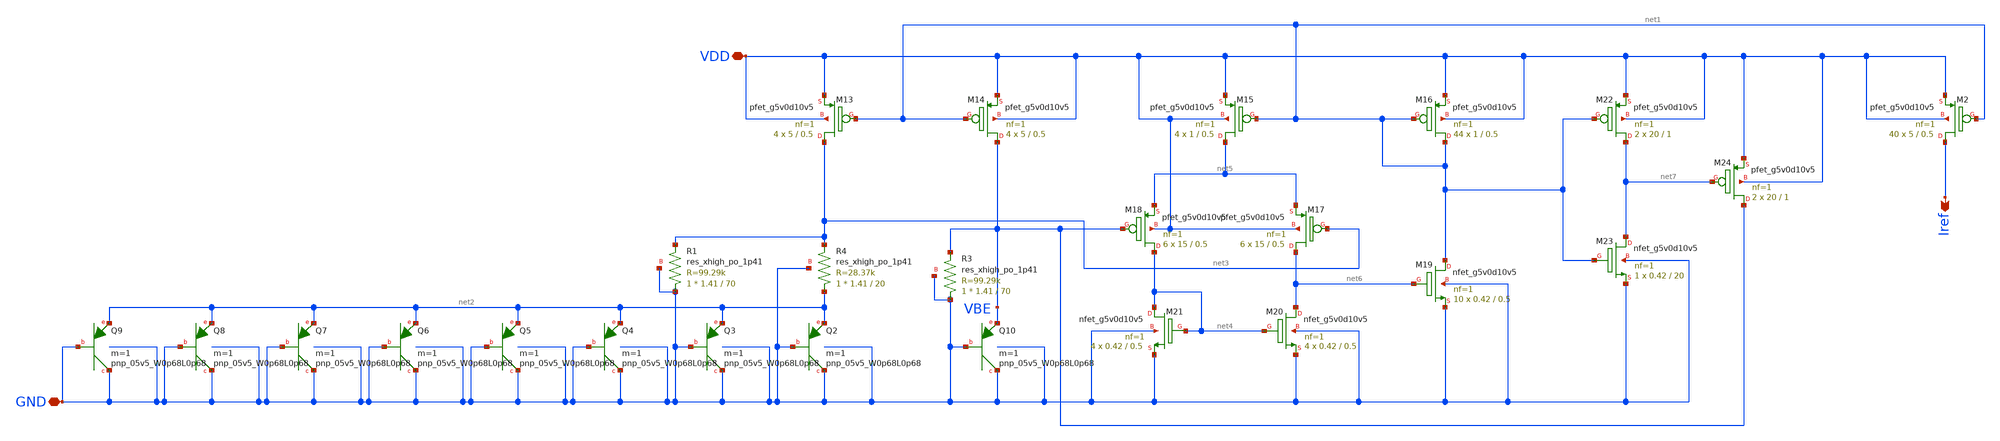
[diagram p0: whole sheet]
** sch_path: pll/lc_vco_lib/Ahmed_Reda/Final Design/BGR_Banba.sch
**.subckt BGR_Banba VDD GND Iref
*.iopin VDD
*.iopin GND
*.opin Iref
XM13 net3 net1 VDD VDD sky130_fd_pr__pfet_g5v0d10v5 L=0.5 W=5 nf=1 ad='int((nf+1)/2) * W/nf * 0.29' as='int((nf+2)/2) * W/nf * 0.29'
+ pd='2*int((nf+1)/2) * (W/nf + 0.29)' ps='2*int((nf+2)/2) * (W/nf + 0.29)' nrd='0.29 / W' nrs='0.29 / W'
+ sa=0 sb=0 sd=0 mult=4 m=4
XM14 VBE net1 VDD VDD sky130_fd_pr__pfet_g5v0d10v5 L=0.5 W=5 nf=1 ad='int((nf+1)/2) * W/nf * 0.29' as='int((nf+2)/2) * W/nf * 0.29'
+ pd='2*int((nf+1)/2) * (W/nf + 0.29)' ps='2*int((nf+2)/2) * (W/nf + 0.29)' nrd='0.29 / W' nrs='0.29 / W'
+ sa=0 sb=0 sd=0 mult=4 m=4
XQ10 GND GND VBE sky130_fd_pr__pnp_05v5_W0p68L0p68 m=1
XQ2 GND GND net2 sky130_fd_pr__pnp_05v5_W0p68L0p68 m=1
XQ3 GND GND net2 sky130_fd_pr__pnp_05v5_W0p68L0p68 m=1
XQ4 GND GND net2 sky130_fd_pr__pnp_05v5_W0p68L0p68 m=1
XQ5 GND GND net2 sky130_fd_pr__pnp_05v5_W0p68L0p68 m=1
XQ6 GND GND net2 sky130_fd_pr__pnp_05v5_W0p68L0p68 m=1
XQ7 GND GND net2 sky130_fd_pr__pnp_05v5_W0p68L0p68 m=1
XQ8 GND GND net2 sky130_fd_pr__pnp_05v5_W0p68L0p68 m=1
XQ9 GND GND net2 sky130_fd_pr__pnp_05v5_W0p68L0p68 m=1
XR4 net2 net3 GND sky130_fd_pr__res_xhigh_po_1p41 L=20 mult=1 m=1
XM15 net5 net1 VDD VDD sky130_fd_pr__pfet_g5v0d10v5 L=0.5 W=1 nf=1 ad='int((nf+1)/2) * W/nf * 0.29' as='int((nf+2)/2) * W/nf * 0.29'
+ pd='2*int((nf+1)/2) * (W/nf + 0.29)' ps='2*int((nf+2)/2) * (W/nf + 0.29)' nrd='0.29 / W' nrs='0.29 / W'
+ sa=0 sb=0 sd=0 mult=4 m=4
XM16 net1 net1 VDD VDD sky130_fd_pr__pfet_g5v0d10v5 L=0.5 W=1 nf=1 ad='int((nf+1)/2) * W/nf * 0.29' as='int((nf+2)/2) * W/nf * 0.29'
+ pd='2*int((nf+1)/2) * (W/nf + 0.29)' ps='2*int((nf+2)/2) * (W/nf + 0.29)' nrd='0.29 / W' nrs='0.29 / W'
+ sa=0 sb=0 sd=0 mult=44 m=44
XM17 net6 net3 net5 VDD sky130_fd_pr__pfet_g5v0d10v5 L=0.5 W=15 nf=1 ad='int((nf+1)/2) * W/nf * 0.29'
+ as='int((nf+2)/2) * W/nf * 0.29' pd='2*int((nf+1)/2) * (W/nf + 0.29)' ps='2*int((nf+2)/2) * (W/nf + 0.29)'
+ nrd='0.29 / W' nrs='0.29 / W' sa=0 sb=0 sd=0 mult=6 m=6
XM18 net4 VBE net5 VDD sky130_fd_pr__pfet_g5v0d10v5 L=0.5 W=15 nf=1 ad='int((nf+1)/2) * W/nf * 0.29'
+ as='int((nf+2)/2) * W/nf * 0.29' pd='2*int((nf+1)/2) * (W/nf + 0.29)' ps='2*int((nf+2)/2) * (W/nf + 0.29)'
+ nrd='0.29 / W' nrs='0.29 / W' sa=0 sb=0 sd=0 mult=6 m=6
XM19 net1 net6 GND GND sky130_fd_pr__nfet_g5v0d10v5 L=0.5 W=0.42 nf=1 ad='int((nf+1)/2) * W/nf * 0.29'
+ as='int((nf+2)/2) * W/nf * 0.29' pd='2*int((nf+1)/2) * (W/nf + 0.29)' ps='2*int((nf+2)/2) * (W/nf + 0.29)'
+ nrd='0.29 / W' nrs='0.29 / W' sa=0 sb=0 sd=0 mult=10 m=10
XM20 net6 net4 GND GND sky130_fd_pr__nfet_g5v0d10v5 L=0.5 W=0.42 nf=1 ad='int((nf+1)/2) * W/nf * 0.29'
+ as='int((nf+2)/2) * W/nf * 0.29' pd='2*int((nf+1)/2) * (W/nf + 0.29)' ps='2*int((nf+2)/2) * (W/nf + 0.29)'
+ nrd='0.29 / W' nrs='0.29 / W' sa=0 sb=0 sd=0 mult=4 m=4
XM21 net4 net4 GND GND sky130_fd_pr__nfet_g5v0d10v5 L=0.5 W=0.42 nf=1 ad='int((nf+1)/2) * W/nf * 0.29'
+ as='int((nf+2)/2) * W/nf * 0.29' pd='2*int((nf+1)/2) * (W/nf + 0.29)' ps='2*int((nf+2)/2) * (W/nf + 0.29)'
+ nrd='0.29 / W' nrs='0.29 / W' sa=0 sb=0 sd=0 mult=4 m=4
XM22 net7 net1 VDD VDD sky130_fd_pr__pfet_g5v0d10v5 L=1 W=20 nf=1 ad='int((nf+1)/2) * W/nf * 0.29' as='int((nf+2)/2) * W/nf * 0.29'
+ pd='2*int((nf+1)/2) * (W/nf + 0.29)' ps='2*int((nf+2)/2) * (W/nf + 0.29)' nrd='0.29 / W' nrs='0.29 / W'
+ sa=0 sb=0 sd=0 mult=2 m=2
XM23 net7 net1 GND GND sky130_fd_pr__nfet_g5v0d10v5 L=20 W=0.42 nf=1 ad='int((nf+1)/2) * W/nf * 0.29'
+ as='int((nf+2)/2) * W/nf * 0.29' pd='2*int((nf+1)/2) * (W/nf + 0.29)' ps='2*int((nf+2)/2) * (W/nf + 0.29)'
+ nrd='0.29 / W' nrs='0.29 / W' sa=0 sb=0 sd=0 mult=1 m=1
XM24 VBE net7 VDD VDD sky130_fd_pr__pfet_g5v0d10v5 L=1 W=20 nf=1 ad='int((nf+1)/2) * W/nf * 0.29' as='int((nf+2)/2) * W/nf * 0.29'
+ pd='2*int((nf+1)/2) * (W/nf + 0.29)' ps='2*int((nf+2)/2) * (W/nf + 0.29)' nrd='0.29 / W' nrs='0.29 / W'
+ sa=0 sb=0 sd=0 mult=2 m=2
XR1 GND net3 GND sky130_fd_pr__res_xhigh_po_1p41 L=70 mult=1 m=1
XR3 GND VBE GND sky130_fd_pr__res_xhigh_po_1p41 L=70 mult=1 m=1
XM2 Iref net1 VDD VDD sky130_fd_pr__pfet_g5v0d10v5 L=0.5 W=5 nf=1 ad='int((nf+1)/2) * W/nf * 0.29' as='int((nf+2)/2) * W/nf * 0.29'
+ pd='2*int((nf+1)/2) * (W/nf + 0.29)' ps='2*int((nf+2)/2) * (W/nf + 0.29)' nrd='0.29 / W' nrs='0.29 / W'
+ sa=0 sb=0 sd=0 mult=40 m=40
**.ends
.end
